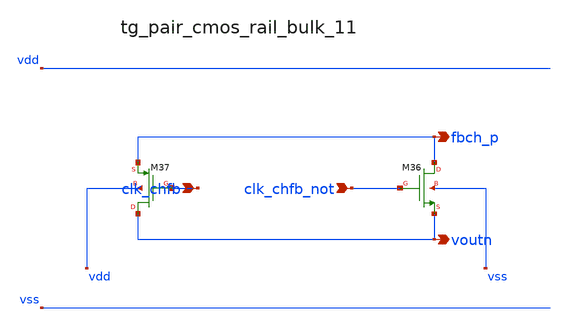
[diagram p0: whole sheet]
** sch_path: analog-db/raw/ia_002_fan_chopper_simple/hier/blocks/tg_pair_cmos_rail_bulk_11.sch
**.subckt tg_pair_cmos_rail_bulk_11 clk_chfb clk_chfb_not fbch_p voutn
*.ipin clk_chfb
*.ipin clk_chfb_not
*.opin fbch_p
*.opin voutn
XM36 fbch_p clk_chfb_not voutn vss sg13_lv_nmos w=x_dut_xm36_w l=x_dut_xm36_l ng=1 m=x_dut_xm36_m
XM37 voutn clk_chfb fbch_p vdd sg13_lv_pmos w=x_dut_xm37_w l=x_dut_xm37_l ng=1 m=x_dut_xm37_m
**.ends
.end
